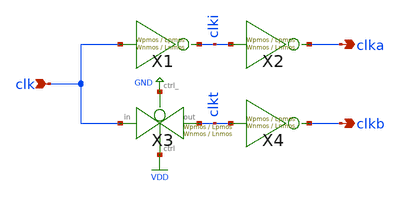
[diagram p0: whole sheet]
** sch_path: xschem/clkgen/comp_clks.sch
**.subckt comp_clks clk clka clkb
*.ipin clk
*.opin clka
*.opin clkb
X3 clk clkt GND VDD transmission_gate Wpmos=Wpmos Lpmos=Lpmos Wnmos=Wnmos Lnmos=Lnmos
X1 clk clki inv Wpmos=Wpmos Lpmos=Lpmos Wnmos=Wnmos Lnmos=Lnmos
X2 clki clka inv Wpmos=Wpmos Lpmos=Lpmos Wnmos=Wnmos Lnmos=Lnmos
X4 clkt clkb inv Wpmos=Wpmos Lpmos=Lpmos Wnmos=Wnmos Lnmos=Lnmos
**.ends

* expanding   symbol:  transmission_gate/transmission_gate.sym # of pins=4
** sym_path: xschem/transmission_gate/transmission_gate.sym
** sch_path: xschem/transmission_gate/transmission_gate.sch
.subckt transmission_gate in out ctrl_ ctrl  Wpmos=0.42 Lpmos=0.18 Wnmos=0.42 Lnmos=0.18
*.iopin in
*.iopin out
*.ipin ctrl_
*.ipin ctrl
XM1 out ctrl in GND sky130_fd_pr__nfet_01v8 L=Lnmos W=Wnmos nf=1 ad='int((nf+1)/2) * W/nf * 0.29' as='int((nf+2)/2) * W/nf * 0.29'
+ pd='2*int((nf+1)/2) * (W/nf + 0.29)' ps='2*int((nf+2)/2) * (W/nf + 0.29)' nrd='0.29 / W' nrs='0.29 / W'
+ sa=0 sb=0 sd=0 mult=1 m=1
XM2 out ctrl_ in VDD sky130_fd_pr__pfet_01v8 L=Lpmos W=Wpmos nf=1 ad='int((nf+1)/2) * W/nf * 0.29' as='int((nf+2)/2) * W/nf * 0.29'
+ pd='2*int((nf+1)/2) * (W/nf + 0.29)' ps='2*int((nf+2)/2) * (W/nf + 0.29)' nrd='0.29 / W' nrs='0.29 / W'
+ sa=0 sb=0 sd=0 mult=1 m=1
.ends


* expanding   symbol:  inv/inv.sym # of pins=2
** sym_path: xschem/inv/inv.sym
** sch_path: xschem/inv/inv.sch
.subckt inv in out  Wpmos=3 Lpmos=0.18 Wnmos=1 Lnmos=0.18
*.ipin in
*.iopin out
XM1 out in GND GND sky130_fd_pr__nfet_01v8 L=Lnmos W=Wnmos nf=1 ad='int((nf+1)/2) * W/nf * 0.29' as='int((nf+2)/2) * W/nf * 0.29'
+ pd='2*int((nf+1)/2) * (W/nf + 0.29)' ps='2*int((nf+2)/2) * (W/nf + 0.29)' nrd='0.29 / W' nrs='0.29 / W'
+ sa=0 sb=0 sd=0 mult=1 m=1
XM2 out in VDD VDD sky130_fd_pr__pfet_01v8 L=Lpmos W=Wpmos nf=1 ad='int((nf+1)/2) * W/nf * 0.29' as='int((nf+2)/2) * W/nf * 0.29'
+ pd='2*int((nf+1)/2) * (W/nf + 0.29)' ps='2*int((nf+2)/2) * (W/nf + 0.29)' nrd='0.29 / W' nrs='0.29 / W'
+ sa=0 sb=0 sd=0 mult=1 m=1
.ends

.GLOBAL VDD
.GLOBAL GND
.end
